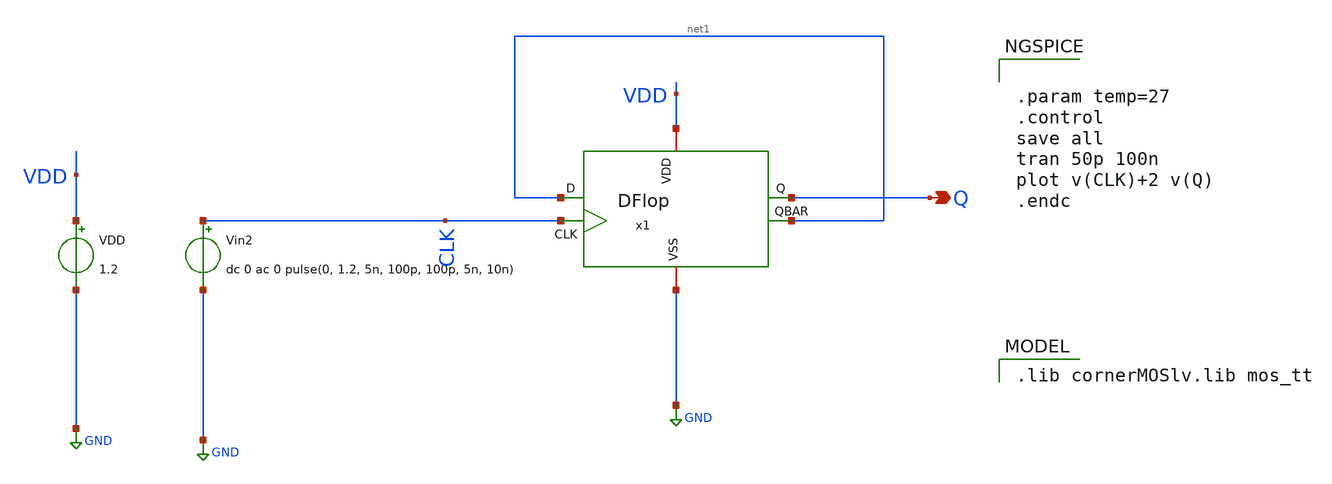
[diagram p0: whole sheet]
** sch_path: Team 1 Design/design_data/xschem/FD(Frequency_Dividers)/Div2F/Div2F_tb.sch
**.subckt Div2F_tb Q
*.opin Q
VDD VDD GND 1.2
Vin2 CLK GND dc 0 ac 0 pulse(0, 1.2, 5n, 100p, 100p, 5n, 10n)
x1 VDD net1 Q CLK net1 GND DFlop
**** begin user architecture code
 .lib cornerMOSlv.lib mos_tt



.param temp=27
.control
save all
tran 50p 100n
plot v(CLK)+2 v(Q)
.endc


**** end user architecture code
**.ends
.GLOBAL GND
.end
